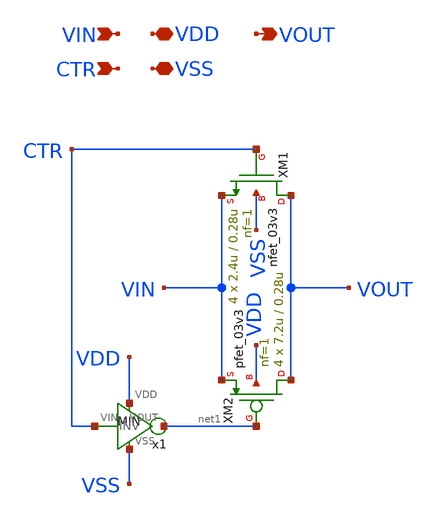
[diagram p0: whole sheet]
** sch_path: ABC123_SDC/design_data/xschem/TGATE/TGATE.sch
**.subckt TGATE VIN VDD VSS CTR VOUT
*.ipin VIN
*.iopin VDD
*.iopin VSS
*.ipin CTR
*.opin VOUT
XM1 VOUT CTR VIN VSS nfet_03v3 L=0.28u W=2.4u nf=1 ad='int((nf+1)/2) * W/nf * 0.18u' as='int((nf+2)/2) * W/nf * 0.18u'
+ pd='2*int((nf+1)/2) * (W/nf + 0.18u)' ps='2*int((nf+2)/2) * (W/nf + 0.18u)' nrd='0.18u / W' nrs='0.18u / W'
+ sa=0 sb=0 sd=0 m=4
XM2 VOUT net1 VIN VDD pfet_03v3 L=0.28u W=7.2u nf=1 ad='int((nf+1)/2) * W/nf * 0.18u' as='int((nf+2)/2) * W/nf * 0.18u'
+ pd='2*int((nf+1)/2) * (W/nf + 0.18u)' ps='2*int((nf+2)/2) * (W/nf + 0.18u)' nrd='0.18u / W' nrs='0.18u / W'
+ sa=0 sb=0 sd=0 m=4
x1 CTR net1 VDD VSS INV
**.ends

* expanding   symbol:  INV/INV.sym # of pins=4
** sym_path: ABC123_SDC/design_data/xschem/INV/INV.sym
** sch_path: ABC123_SDC/design_data/xschem/INV/INV.sch
.subckt INV VIN VOUT VDD VSS
*.ipin VIN
*.iopin VDD
*.iopin VSS
*.opin VOUT
XM1 VOUT VIN VDD VDD pfet_03v3 L=0.28u W=1.87u nf=1 ad='int((nf+1)/2) * W/nf * 0.18u' as='int((nf+2)/2) * W/nf * 0.18u'
+ pd='2*int((nf+1)/2) * (W/nf + 0.18u)' ps='2*int((nf+2)/2) * (W/nf + 0.18u)' nrd='0.18u / W' nrs='0.18u / W'
+ sa=0 sb=0 sd=0 m=1
XM2 VOUT VIN VSS VSS nfet_03v3 L=0.28u W=1.87u nf=1 ad='int((nf+1)/2) * W/nf * 0.18u' as='int((nf+2)/2) * W/nf * 0.18u'
+ pd='2*int((nf+1)/2) * (W/nf + 0.18u)' ps='2*int((nf+2)/2) * (W/nf + 0.18u)' nrd='0.18u / W' nrs='0.18u / W'
+ sa=0 sb=0 sd=0 m=1
.ends

.end
